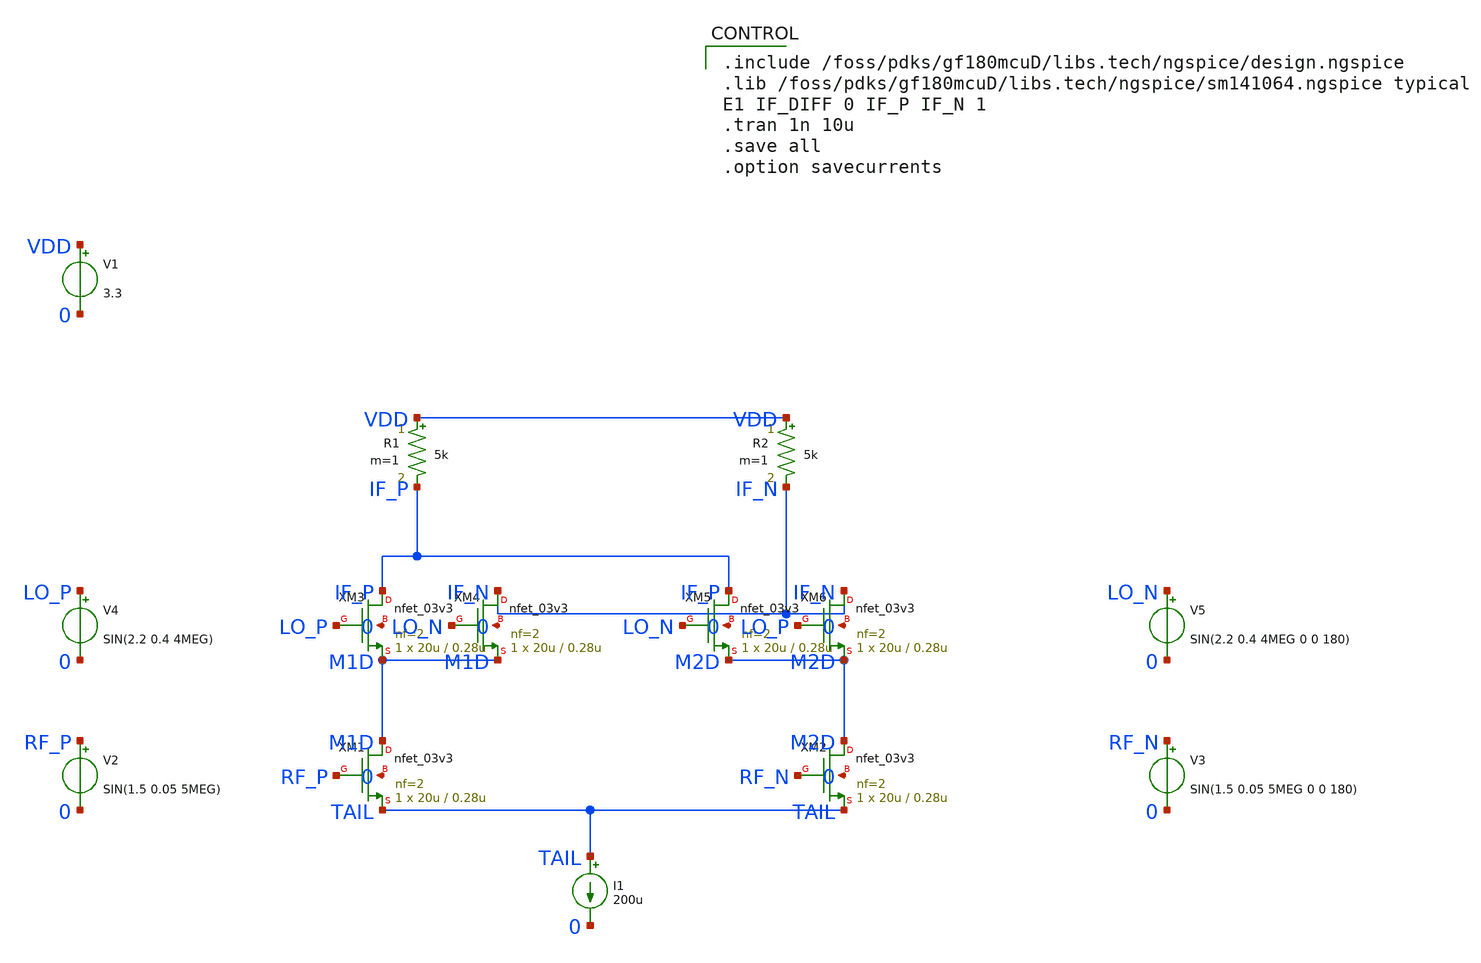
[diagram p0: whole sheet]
** sch_path: modules/PandaChip/designs/dbm/dbm_tb.sch
**.subckt dbm_tb
XM1 M1D RF_P TAIL 0 nfet_03v3 L=0.28u W=20u nf=2 ad='int((nf+1)/2) * W/nf * 0.18u' as='int((nf+2)/2) * W/nf * 0.18u'
+ pd='2*int((nf+1)/2) * (W/nf + 0.18u)' ps='2*int((nf+2)/2) * (W/nf + 0.18u)' nrd='0.18u / W' nrs='0.18u / W'
+ sa=0 sb=0 sd=0 m=1
XM2 M2D RF_N TAIL 0 nfet_03v3 L=0.28u W=20u nf=2 ad='int((nf+1)/2) * W/nf * 0.18u' as='int((nf+2)/2) * W/nf * 0.18u'
+ pd='2*int((nf+1)/2) * (W/nf + 0.18u)' ps='2*int((nf+2)/2) * (W/nf + 0.18u)' nrd='0.18u / W' nrs='0.18u / W'
+ sa=0 sb=0 sd=0 m=1
XM3 IF_P LO_P M1D 0 nfet_03v3 L=0.28u W=20u nf=2 ad='int((nf+1)/2) * W/nf * 0.18u' as='int((nf+2)/2) * W/nf * 0.18u'
+ pd='2*int((nf+1)/2) * (W/nf + 0.18u)' ps='2*int((nf+2)/2) * (W/nf + 0.18u)' nrd='0.18u / W' nrs='0.18u / W'
+ sa=0 sb=0 sd=0 m=1
XM4 IF_N LO_N M1D 0 nfet_03v3 L=0.28u W=20u nf=2 ad='int((nf+1)/2) * W/nf * 0.18u' as='int((nf+2)/2) * W/nf * 0.18u'
+ pd='2*int((nf+1)/2) * (W/nf + 0.18u)' ps='2*int((nf+2)/2) * (W/nf + 0.18u)' nrd='0.18u / W' nrs='0.18u / W'
+ sa=0 sb=0 sd=0 m=1
XM5 IF_P LO_N M2D 0 nfet_03v3 L=0.28u W=20u nf=2 ad='int((nf+1)/2) * W/nf * 0.18u' as='int((nf+2)/2) * W/nf * 0.18u'
+ pd='2*int((nf+1)/2) * (W/nf + 0.18u)' ps='2*int((nf+2)/2) * (W/nf + 0.18u)' nrd='0.18u / W' nrs='0.18u / W'
+ sa=0 sb=0 sd=0 m=1
XM6 IF_N LO_P M2D 0 nfet_03v3 L=0.28u W=20u nf=2 ad='int((nf+1)/2) * W/nf * 0.18u' as='int((nf+2)/2) * W/nf * 0.18u'
+ pd='2*int((nf+1)/2) * (W/nf + 0.18u)' ps='2*int((nf+2)/2) * (W/nf + 0.18u)' nrd='0.18u / W' nrs='0.18u / W'
+ sa=0 sb=0 sd=0 m=1
R1 VDD IF_P 5k m=1
R2 VDD IF_N 5k m=1
I1 TAIL 0 200u
V1 VDD 0 3.3
V2 RF_P 0 SIN(1.5 0.05 5MEG)
V3 RF_N 0 SIN(1.5 0.05 5MEG 0 0 180)
V4 LO_P 0 SIN(2.2 0.4 4MEG)
V5 LO_N 0 SIN(2.2 0.4 4MEG 0 0 180)
**** begin user architecture code

.include /foss/pdks/gf180mcuD/libs.tech/ngspice/design.ngspice
.lib /foss/pdks/gf180mcuD/libs.tech/ngspice/sm141064.ngspice typical
E1 IF_DIFF 0 IF_P IF_N 1
.tran 1n 10u
.save all
.option savecurrents

**** end user architecture code
**.ends
.end
